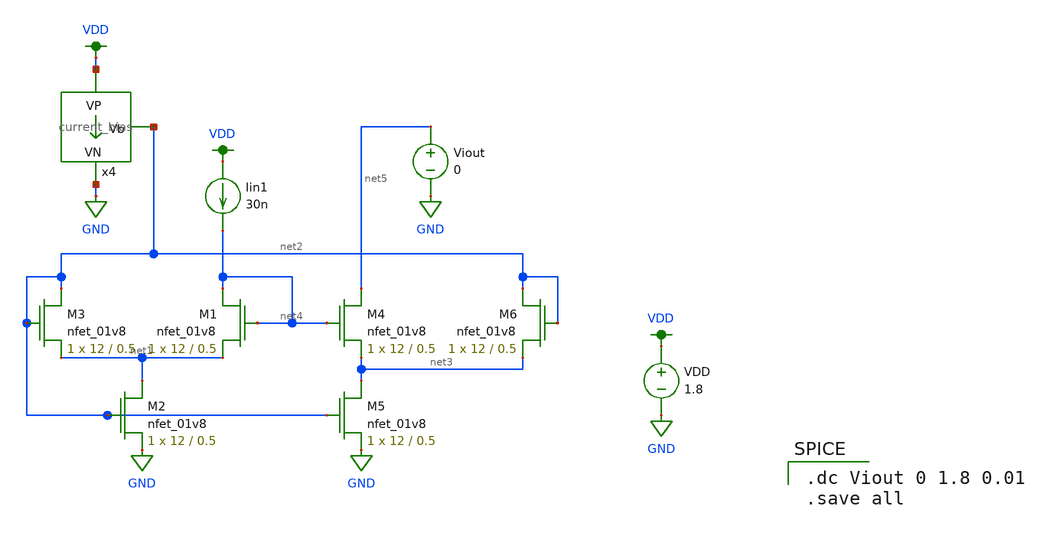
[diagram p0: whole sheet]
** sch_path: Final DAC files/current mirrors/Brads_low_voltage_current_mirror.sch
**.subckt Brads_low_voltage_current_mirror
Viout net5 GND 0
VDD VDD GND 1.8
x4 VDD net2 GND current_bias
XM3 net2 net2 net1 GND sky130_fd_pr__nfet_01v8 L=0.5 W=12 nf=1 ad='int((nf+1)/2) * W/nf * 0.29' as='int((nf+2)/2) * W/nf * 0.29'
+ pd='2*int((nf+1)/2) * (W/nf + 0.29)' ps='2*int((nf+2)/2) * (W/nf + 0.29)' nrd='0.29 / W' nrs='0.29 / W'
+ sa=0 sb=0 sd=0 mult=1 m=1
XM1 net4 net4 net1 GND sky130_fd_pr__nfet_01v8 L=0.5 W=12 nf=1 ad='int((nf+1)/2) * W/nf * 0.29' as='int((nf+2)/2) * W/nf * 0.29'
+ pd='2*int((nf+1)/2) * (W/nf + 0.29)' ps='2*int((nf+2)/2) * (W/nf + 0.29)' nrd='0.29 / W' nrs='0.29 / W'
+ sa=0 sb=0 sd=0 mult=1 m=1
XM2 net1 net2 GND GND sky130_fd_pr__nfet_01v8 L=0.5 W=12 nf=1 ad='int((nf+1)/2) * W/nf * 0.29' as='int((nf+2)/2) * W/nf * 0.29'
+ pd='2*int((nf+1)/2) * (W/nf + 0.29)' ps='2*int((nf+2)/2) * (W/nf + 0.29)' nrd='0.29 / W' nrs='0.29 / W'
+ sa=0 sb=0 sd=0 mult=1 m=1
XM4 net5 net4 net3 GND sky130_fd_pr__nfet_01v8 L=0.5 W=12 nf=1 ad='int((nf+1)/2) * W/nf * 0.29' as='int((nf+2)/2) * W/nf * 0.29'
+ pd='2*int((nf+1)/2) * (W/nf + 0.29)' ps='2*int((nf+2)/2) * (W/nf + 0.29)' nrd='0.29 / W' nrs='0.29 / W'
+ sa=0 sb=0 sd=0 mult=1 m=1
XM5 net3 net2 GND GND sky130_fd_pr__nfet_01v8 L=0.5 W=12 nf=1 ad='int((nf+1)/2) * W/nf * 0.29' as='int((nf+2)/2) * W/nf * 0.29'
+ pd='2*int((nf+1)/2) * (W/nf + 0.29)' ps='2*int((nf+2)/2) * (W/nf + 0.29)' nrd='0.29 / W' nrs='0.29 / W'
+ sa=0 sb=0 sd=0 mult=1 m=1
XM6 net2 net2 net3 GND sky130_fd_pr__nfet_01v8 L=0.5 W=12 nf=1 ad='int((nf+1)/2) * W/nf * 0.29' as='int((nf+2)/2) * W/nf * 0.29'
+ pd='2*int((nf+1)/2) * (W/nf + 0.29)' ps='2*int((nf+2)/2) * (W/nf + 0.29)' nrd='0.29 / W' nrs='0.29 / W'
+ sa=0 sb=0 sd=0 mult=1 m=1
Iin1 VDD net4 30n
**** begin user architecture code

.option wnflag=1
.param MC_SWITCH=0.0
.lib ~/skywater/skywater-pdk/libraries/sky130_fd_pr_ngspice/latest/models/sky130.lib.spice tt


.dc Viout 0 1.8 0.01
.save all

**** end user architecture code
**.ends
.GLOBAL GND
.GLOBAL VDD
.end
